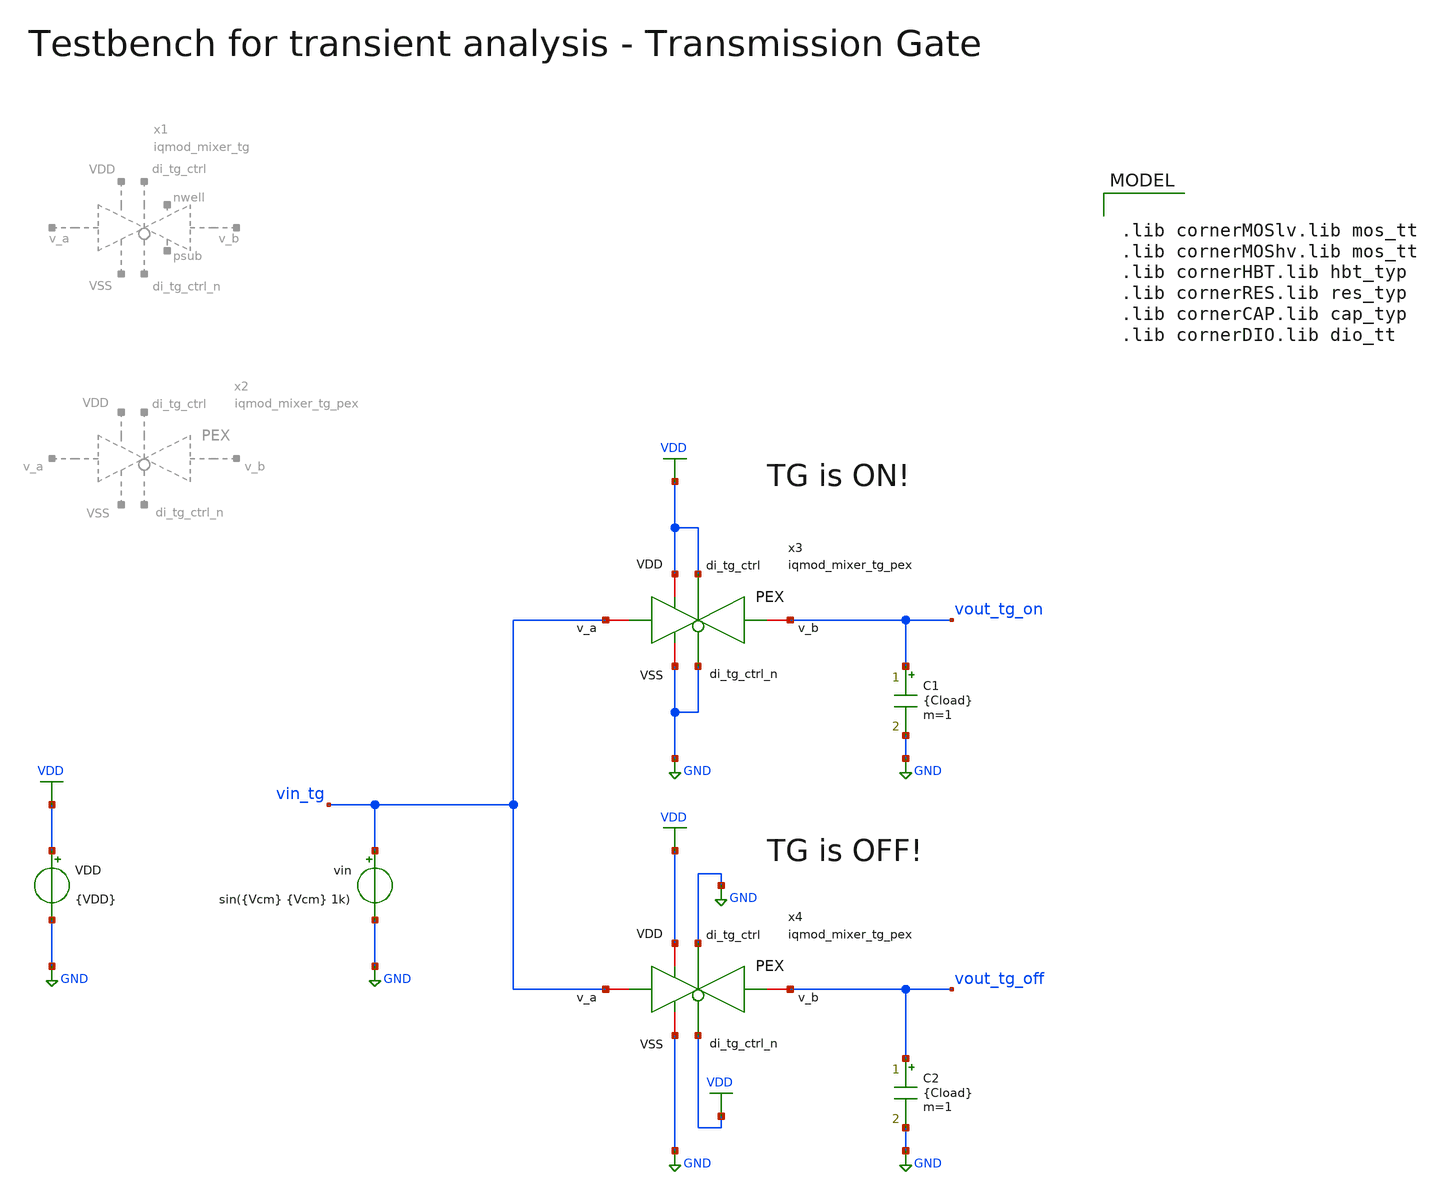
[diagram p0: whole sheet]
** sch_path: ihp130/macros/iqmod/xschem/testbenches/iqmod_mixer_tg_tb_tran.sch
**.subckt iqmod_mixer_tg_tb_tran
VDD VDD GND {VDD}
vin vin_tg GND sin({Vcm} {Vcm} 1k)
C1 vout_tg_on GND {Cload} m=1
C2 vout_tg_off GND {Cload} m=1
x3 VDD GND GND VDD vin_tg vout_tg_on iqmod_mixer_tg_pex
x4 VDD VDD GND GND vin_tg vout_tg_off iqmod_mixer_tg_pex
**** begin user architecture code


.include ../../verification/pex/iqmod_mixer_tg_pex.spice
.param VDD=1.5
.param Vcm=VDD/2
.param temp=27
.param Cload=10p
.options savecurrents klu method=gear reltol=1e-3 abstol=1e-15 gmin=1e-15
.control

save all

* Operating Point Analysis
op
remzerovec
write iqmod_mixer_tg_tb_tran.raw
set appendwrite

* Transient Analysis
tran 10u 10ms
write iqmod_mixer_tg_tb_tran.raw

plot vin_tg vout_tg_on
plot vin_tg vout_tg_off

* Writing Data
unset appendwrite
set wr_singlescale
set wr_vecnames
wrdata $PROJECT_PATH/python/plot_simulations/data/iqmod_mixer_tg_tb_tran.txt v(vin_tg) v(vout_tg_on)
+ v(vout_tg_off)


*quit
.endc


.lib cornerMOSlv.lib mos_tt
.lib cornerMOShv.lib mos_tt
.lib cornerHBT.lib hbt_typ
.lib cornerRES.lib res_typ
.lib cornerCAP.lib cap_typ
.lib cornerDIO.lib dio_tt

**** end user architecture code
**.ends

* expanding   symbol:  iqmod_mixer_tg.sym # of pins=8
** sym_path: ihp130/macros/iqmod/xschem/iqmod_mixer_tg.sym
** sch_path: ihp130/macros/iqmod/xschem/iqmod_mixer_tg.sch
.subckt iqmod_mixer_tg nwell psub VDD di_tg_ctrl VSS v_b v_a di_tg_ctrl_n
*.iopin v_a
*.iopin v_b
*.ipin di_tg_ctrl
*.ipin di_tg_ctrl_n
*.iopin VDD
*.iopin VSS
*.iopin nwell
*.iopin psub
XM1 v_a di_tg_ctrl v_b psub sg13_lv_nmos w=108.0u l=0.13u ng=36 m=1 mm_ok=1
XM2 v_a di_tg_ctrl_n v_b nwell sg13_lv_pmos w=324.0u l=0.13u ng=36 m=1 mm_ok=1
XMdummy2 v_b di_tg_ctrl v_b nwell sg13_lv_pmos w=162.0u l=0.13u ng=18 m=1 mm_ok=1
XMdummy1 v_b di_tg_ctrl_n v_b psub sg13_lv_nmos w=54.0u l=0.13u ng=18 m=1 mm_ok=1
XR1 VDD nwell ntap1 R=2.829 w=29.86e-6 l=11.02e-6 rw=0.3e-6
XR2 VSS psub ptap1 R=3.29 w=29.86e-6 l=5.38e-6 rw=0.3e-6
.ends

.GLOBAL GND
.GLOBAL VDD
.end
